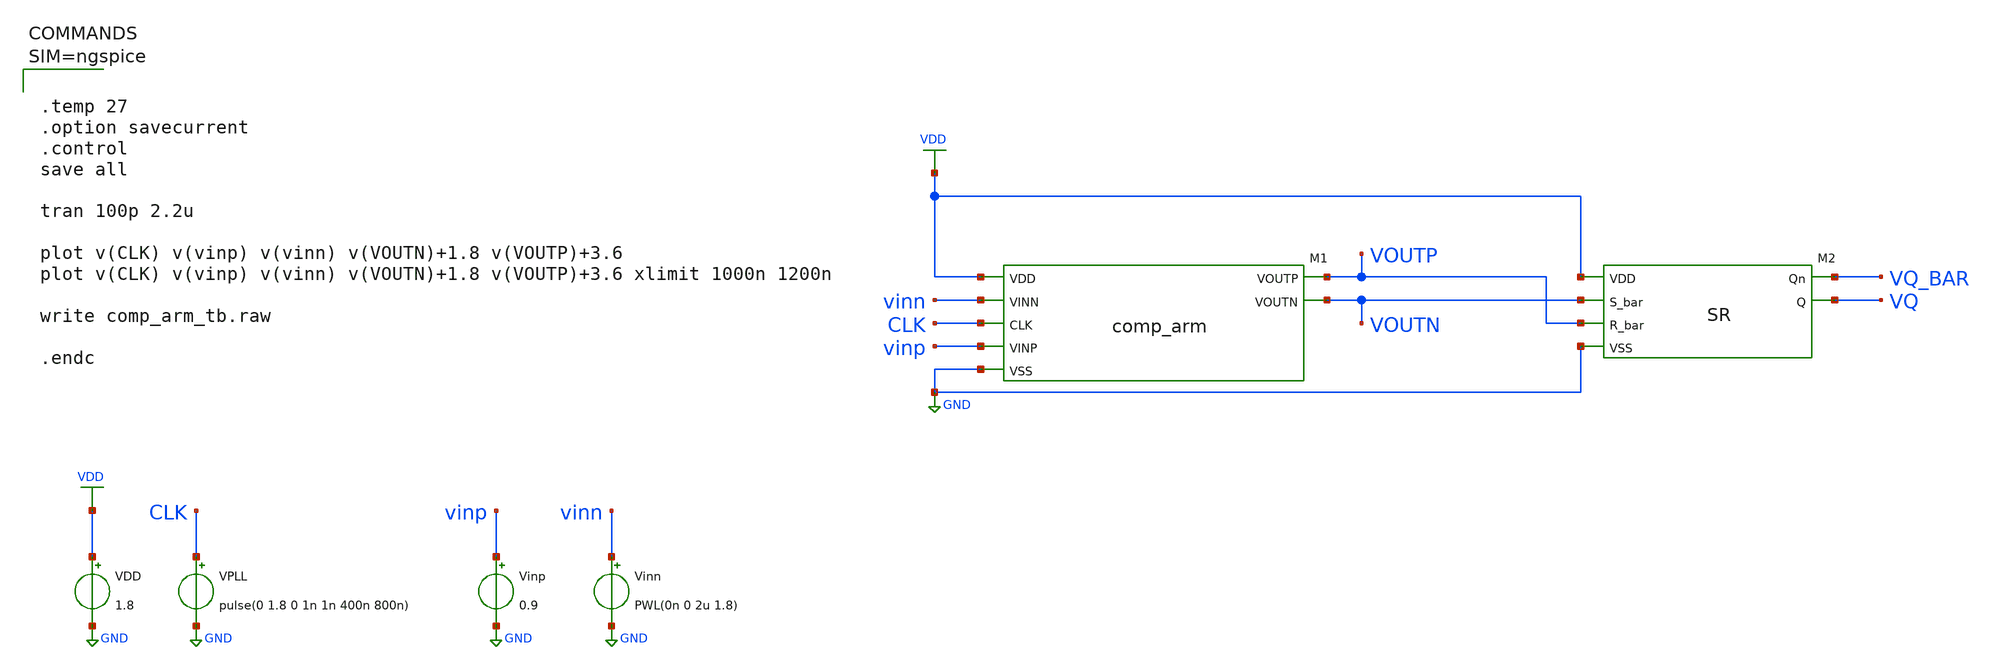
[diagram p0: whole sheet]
** sch_path: SKY130/SAR-ADC/SAR-ADC_1.8V/comp_arm_tb.sch
**.subckt comp_arm_tb
VDD VDD GND 1.8
Vinn vinn GND PWL(0n 0 2u 1.8)
Vinp vinp GND 0.9
VPLL CLK GND pulse(0 1.8 0 1n 1n 400n 800n)
XM2 VDD VQ_BAR VQ VOUTP VOUTN GND SR
XM1 VOUTP VDD vinp vinn CLK GND VOUTN comp_arm
**** begin user architecture code

** opencircuitdesign pdks install
.lib $::SKYWATER_MODELS/sky130.lib.spice tt




.temp 27
.option savecurrent
.control
save all

tran 100p 2.2u

plot v(CLK) v(vinp) v(vinn) v(VOUTN)+1.8 v(VOUTP)+3.6
plot v(CLK) v(vinp) v(vinn) v(VOUTN)+1.8 v(VOUTP)+3.6 xlimit 1000n 1200n

write comp_arm_tb.raw

.endc



**** end user architecture code
**.ends
.GLOBAL GND
.GLOBAL VDD
.end
